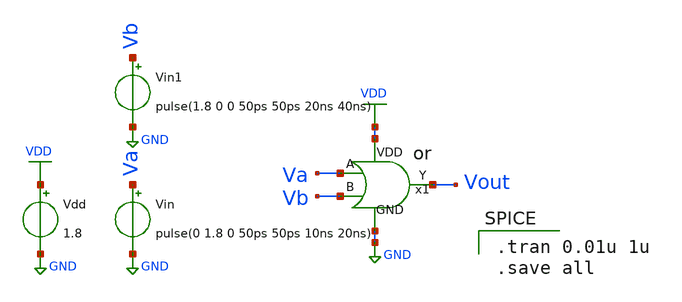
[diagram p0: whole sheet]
** sch_path: designs/or/xschem/or_tb.sch
**.subckt or_tb
Vdd VDD GND 1.8
Vin Va GND pulse(0 1.8 0 50ps 50ps 10ns 20ns)
Vin1 Vb GND pulse(1.8 0 0 50ps 50ps 20ns 40ns)
x1 VDD Va Vout Vb GND or
**** begin user architecture code

** opencircuidesign pdks install
.lib /home/ubvm/Desktop/chip_design/open_pdks/sky130/sky130A/libs.tech/ngspice/sky130.lib.spice tt_mm




.tran 0.01u 1u
.save all

**** end user architecture code
**.ends

* expanding   symbol:  /home/ubvm/unic-cass/xschem/or/or.sym # of pins=5
** sym_path: designs/or/xschem/or.sym
** sch_path: designs/or/xschem/or.sch
.subckt or VDD A Y B GND
input p1
output p2
inout p3
inout p4
input p5
XM1 net7 net5 net3 net3 sky130_fd_pr__nfet_01v8 L=0.15 W=1 nf=1 ad='int((1 + 1)/2) * 1 / 1 * 0.29' as='int((1 + 2)/2) * 1 / 1 * 0.29'
+ pd='2*int((1 + 1)/2) * (1 / 1 + 0.29)' ps='2*int((1 + 2)/2) * (1 / 1 + 0.29)' nrd='0.29 / 1 ' nrs='0.29 / 1 '
+ sa=0 sb=0 sd=0 mult=1 m=1
XM2 net1 net7 net2 net2 sky130_fd_pr__pfet_01v8 L=0.15 W=1 nf=1 ad='int((1 + 1)/2) * 1 / 1 * 0.29' as='int((1 + 2)/2) * 1 / 1 * 0.29'
+ pd='2*int((1 + 1)/2) * (1 / 1 + 0.29)' ps='2*int((1 + 2)/2) * (1 / 1 + 0.29)' nrd='0.29 / 1 ' nrs='0.29 / 1 '
+ sa=0 sb=0 sd=0 mult=1 m=1
XM3 net7 net4 net3 net3 sky130_fd_pr__nfet_01v8 L=0.15 W=1 nf=1 ad='int((1 + 1)/2) * 1 / 1 * 0.29' as='int((1 + 2)/2) * 1 / 1 * 0.29'
+ pd='2*int((1 + 1)/2) * (1 / 1 + 0.29)' ps='2*int((1 + 2)/2) * (1 / 1 + 0.29)' nrd='0.29 / 1 ' nrs='0.29 / 1 '
+ sa=0 sb=0 sd=0 mult=1 m=1
XM4 net6 net4 net2 net2 sky130_fd_pr__pfet_01v8 L=0.15 W=1 nf=1 ad='int((1 + 1)/2) * 1 / 1 * 0.29' as='int((1 + 2)/2) * 1 / 1 * 0.29'
+ pd='2*int((1 + 1)/2) * (1 / 1 + 0.29)' ps='2*int((1 + 2)/2) * (1 / 1 + 0.29)' nrd='0.29 / 1 ' nrs='0.29 / 1 '
+ sa=0 sb=0 sd=0 mult=1 m=1
XM5 net7 net5 net6 net6 sky130_fd_pr__pfet_01v8 L=0.15 W=1 nf=1 ad='int((1 + 1)/2) * 1 / 1 * 0.29' as='int((1 + 2)/2) * 1 / 1 * 0.29'
+ pd='2*int((1 + 1)/2) * (1 / 1 + 0.29)' ps='2*int((1 + 2)/2) * (1 / 1 + 0.29)' nrd='0.29 / 1 ' nrs='0.29 / 1 '
+ sa=0 sb=0 sd=0 mult=1 m=1
XM6 net1 net7 net3 net3 sky130_fd_pr__nfet_01v8 L=0.15 W=1 nf=1 ad='int((1 + 1)/2) * 1 / 1 * 0.29' as='int((1 + 2)/2) * 1 / 1 * 0.29'
+ pd='2*int((1 + 1)/2) * (1 / 1 + 0.29)' ps='2*int((1 + 2)/2) * (1 / 1 + 0.29)' nrd='0.29 / 1 ' nrs='0.29 / 1 '
+ sa=0 sb=0 sd=0 mult=1 m=1
.ends

.GLOBAL VDD
.GLOBAL GND
.end
